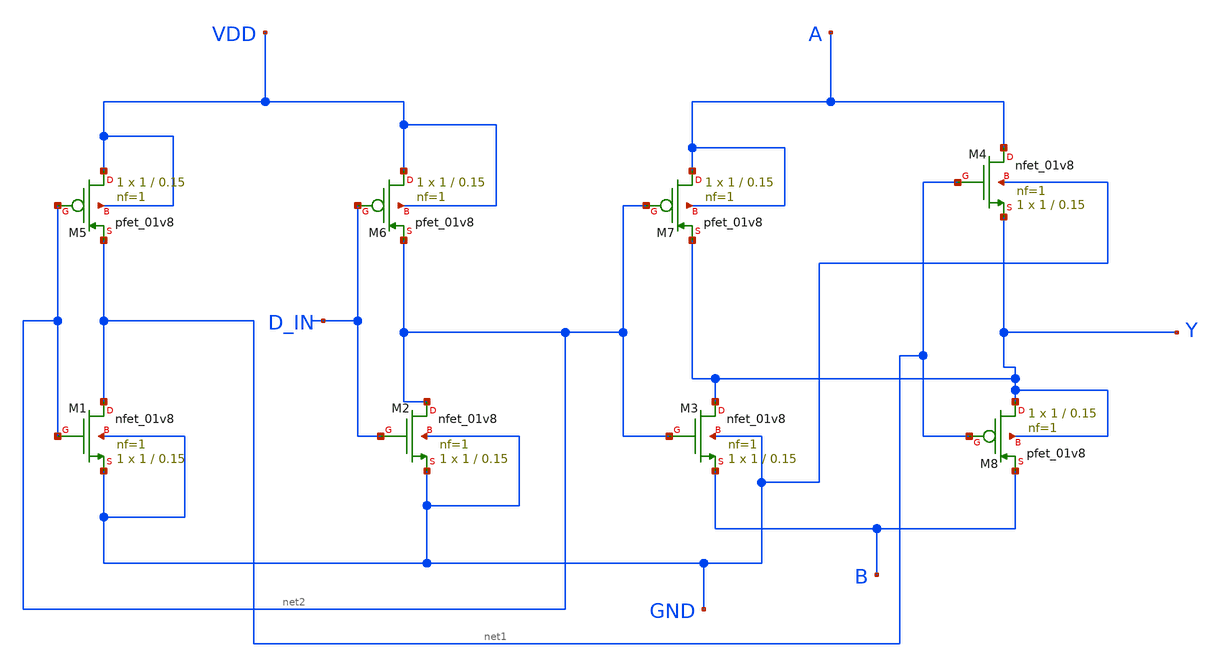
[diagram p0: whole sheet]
** sch_path: mag/SW.sch
**.subckt SW
XM1 net1 net2 GND GND sky130_fd_pr__nfet_01v8 L=0.15 W=1 nf=1 ad='W * 0.29' as='W * 0.29' pd='W + 2 * 0.29'
+ ps='W + 2 * 0.29' nrd=0 nrs=0 sa=0 sb=0 sd=0 mult=1 m=1
XM2 net2 D_IN GND GND sky130_fd_pr__nfet_01v8 L=0.15 W=1 nf=1 ad='W * 0.29' as='W * 0.29' pd='W + 2 * 0.29'
+ ps='W + 2 * 0.29' nrd=0 nrs=0 sa=0 sb=0 sd=0 mult=1 m=1
XM3 Y net2 B GND sky130_fd_pr__nfet_01v8 L=0.15 W=1 nf=1 ad='W * 0.29' as='W * 0.29' pd='W + 2 * 0.29'
+ ps='W + 2 * 0.29' nrd=0 nrs=0 sa=0 sb=0 sd=0 mult=1 m=1
XM4 A net1 Y GND sky130_fd_pr__nfet_01v8 L=0.15 W=1 nf=1 ad='W * 0.29' as='W * 0.29' pd='W + 2 * 0.29'
+ ps='W + 2 * 0.29' nrd=0 nrs=0 sa=0 sb=0 sd=0 mult=1 m=1
XM5 VDD net2 net1 VDD sky130_fd_pr__pfet_01v8 L=0.15 W=1 nf=1 ad='W * 0.29' as='W * 0.29' pd='W + 2 * 0.29'
+ ps='W + 2 * 0.29' nrd=0 nrs=0 sa=0 sb=0 sd=0 mult=1 m=1
XM6 VDD D_IN net2 VDD sky130_fd_pr__pfet_01v8 L=0.15 W=1 nf=1 ad='W * 0.29' as='W * 0.29' pd='W + 2 * 0.29'
+ ps='W + 2 * 0.29' nrd=0 nrs=0 sa=0 sb=0 sd=0 mult=1 m=1
XM7 A net2 Y A sky130_fd_pr__pfet_01v8 L=0.15 W=1 nf=1 ad='W * 0.29' as='W * 0.29' pd='W + 2 * 0.29'
+ ps='W + 2 * 0.29' nrd=0 nrs=0 sa=0 sb=0 sd=0 mult=1 m=1
XM8 Y net1 B Y sky130_fd_pr__pfet_01v8 L=0.15 W=1 nf=1 ad='W * 0.29' as='W * 0.29' pd='W + 2 * 0.29'
+ ps='W + 2 * 0.29' nrd=0 nrs=0 sa=0 sb=0 sd=0 mult=1 m=1
**.ends
.end
